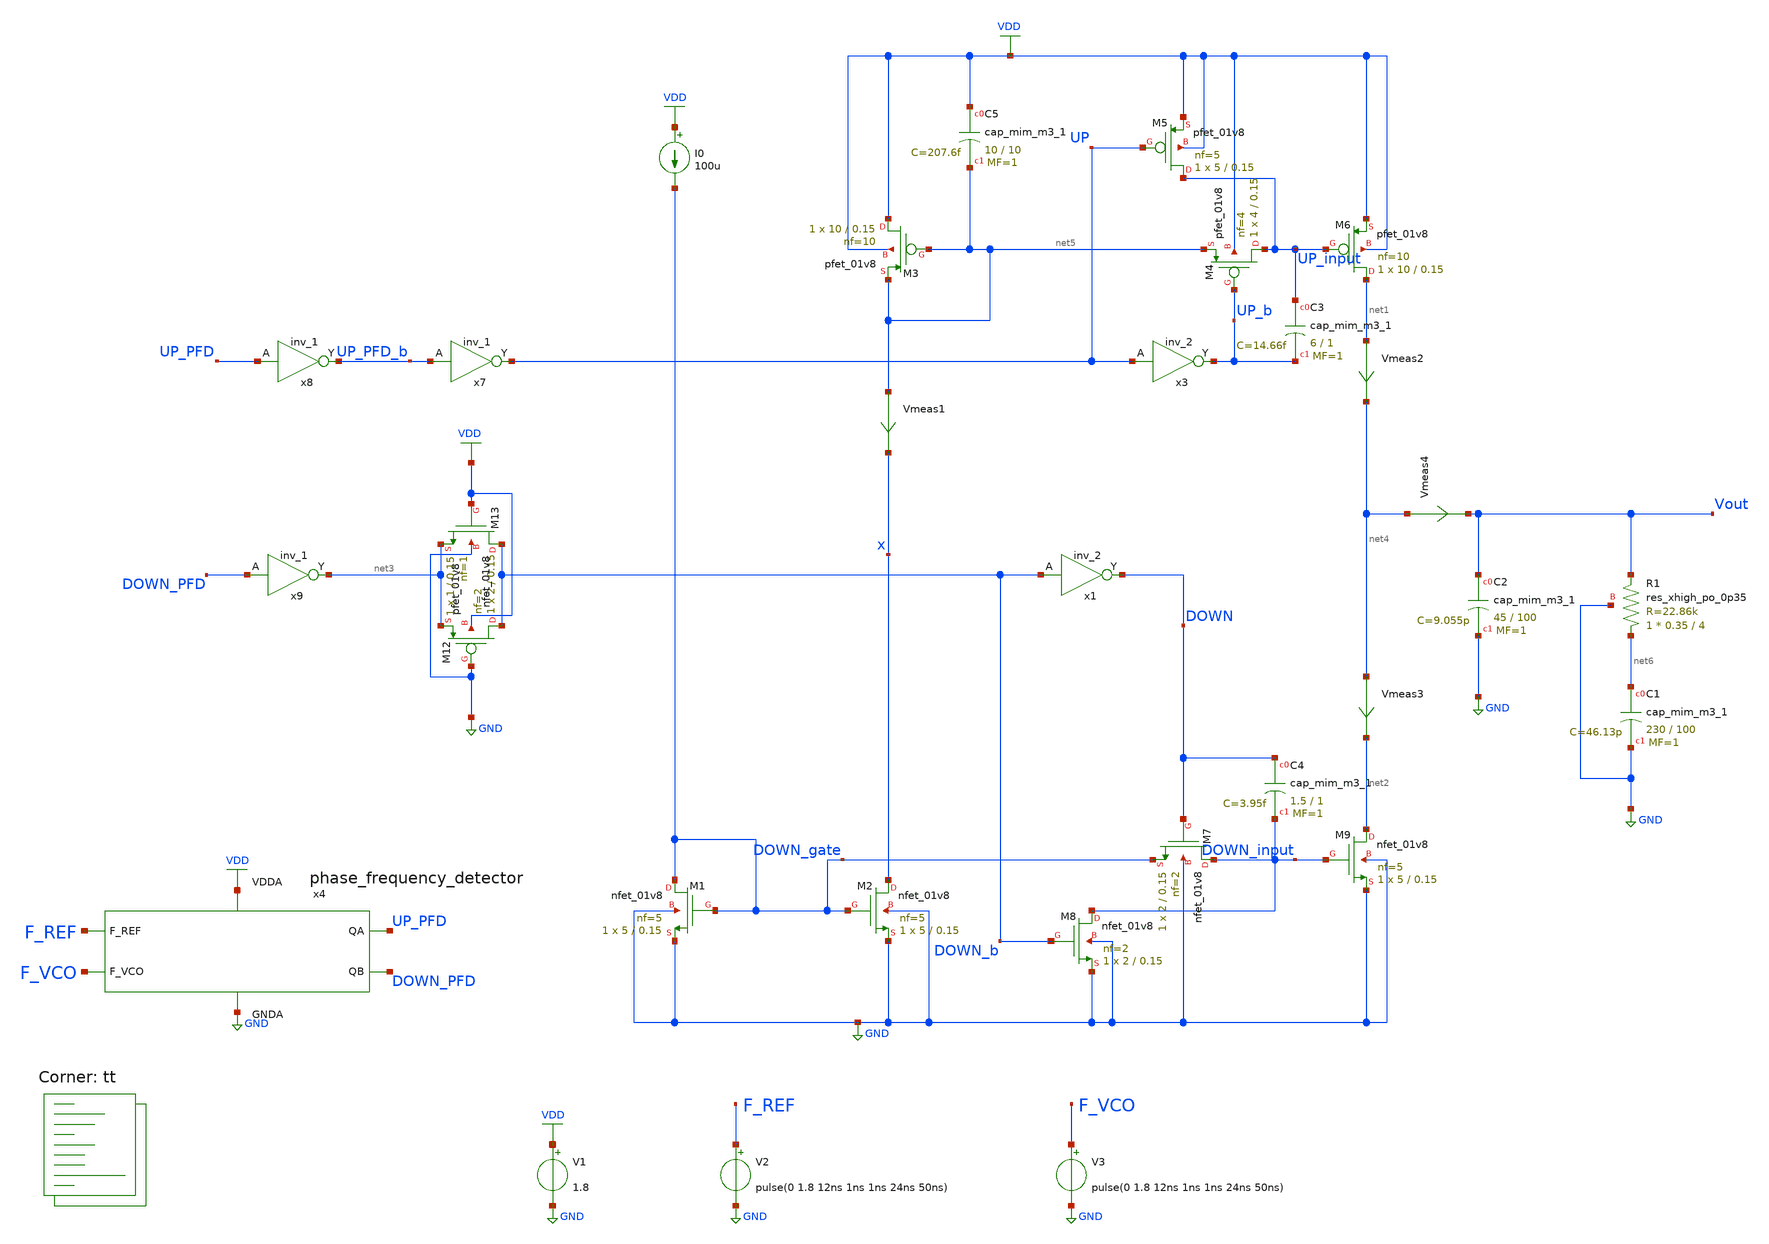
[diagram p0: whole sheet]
** sch_path: projects/pll/charge_pump/xschem_ngspice/pfd_charge_pump_5.sch
**.subckt pfd_charge_pump_5
XM1 DOWN_gate DOWN_gate GND GND sky130_fd_pr__nfet_01v8 L=0.15 W=5 nf=5 ad='int((nf+1)/2) * W/nf * 0.29'
+ as='int((nf+2)/2) * W/nf * 0.29' pd='2*int((nf+1)/2) * (W/nf + 0.29)' ps='2*int((nf+2)/2) * (W/nf + 0.29)'
+ nrd='0.29 / W' nrs='0.29 / W' sa=0 sb=0 sd=0 mult=1 m=1
XM2 x DOWN_gate GND GND sky130_fd_pr__nfet_01v8 L=0.15 W=5 nf=5 ad='int((nf+1)/2) * W/nf * 0.29' as='int((nf+2)/2) * W/nf * 0.29'
+ pd='2*int((nf+1)/2) * (W/nf + 0.29)' ps='2*int((nf+2)/2) * (W/nf + 0.29)' nrd='0.29 / W' nrs='0.29 / W'
+ sa=0 sb=0 sd=0 mult=1 m=1
XM3 VDD net5 net5 VDD sky130_fd_pr__pfet_01v8 L=0.15 W=10 nf=10 ad='int((nf+1)/2) * W/nf * 0.29' as='int((nf+2)/2) * W/nf * 0.29'
+ pd='2*int((nf+1)/2) * (W/nf + 0.29)' ps='2*int((nf+2)/2) * (W/nf + 0.29)' nrd='0.29 / W' nrs='0.29 / W'
+ sa=0 sb=0 sd=0 mult=1 m=1
V1 VDD GND 1.8
I0 VDD DOWN_gate 100u
Vmeas1 net5 x 0
.save i(vmeas1)
XM4 UP_input UP_b net5 VDD sky130_fd_pr__pfet_01v8 L=0.15 W=4 nf=4 ad='int((nf+1)/2) * W/nf * 0.29' as='int((nf+2)/2) * W/nf * 0.29'
+ pd='2*int((nf+1)/2) * (W/nf + 0.29)' ps='2*int((nf+2)/2) * (W/nf + 0.29)' nrd='0.29 / W' nrs='0.29 / W'
+ sa=0 sb=0 sd=0 mult=1 m=1
XM5 UP_input UP VDD VDD sky130_fd_pr__pfet_01v8 L=0.15 W=5 nf=5 ad='int((nf+1)/2) * W/nf * 0.29' as='int((nf+2)/2) * W/nf * 0.29'
+ pd='2*int((nf+1)/2) * (W/nf + 0.29)' ps='2*int((nf+2)/2) * (W/nf + 0.29)' nrd='0.29 / W' nrs='0.29 / W'
+ sa=0 sb=0 sd=0 mult=1 m=1
XM6 net1 UP_input VDD VDD sky130_fd_pr__pfet_01v8 L=0.15 W=10 nf=10 ad='int((nf+1)/2) * W/nf * 0.29'
+ as='int((nf+2)/2) * W/nf * 0.29' pd='2*int((nf+1)/2) * (W/nf + 0.29)' ps='2*int((nf+2)/2) * (W/nf + 0.29)'
+ nrd='0.29 / W' nrs='0.29 / W' sa=0 sb=0 sd=0 mult=1 m=1
Vmeas2 net1 net4 0
.save i(vmeas2)
XM7 DOWN_input DOWN DOWN_gate GND sky130_fd_pr__nfet_01v8 L=0.15 W=2 nf=2 ad='int((nf+1)/2) * W/nf * 0.29'
+ as='int((nf+2)/2) * W/nf * 0.29' pd='2*int((nf+1)/2) * (W/nf + 0.29)' ps='2*int((nf+2)/2) * (W/nf + 0.29)'
+ nrd='0.29 / W' nrs='0.29 / W' sa=0 sb=0 sd=0 mult=1 m=1
XM8 DOWN_input DOWN_b GND GND sky130_fd_pr__nfet_01v8 L=0.15 W=2 nf=2 ad='int((nf+1)/2) * W/nf * 0.29'
+ as='int((nf+2)/2) * W/nf * 0.29' pd='2*int((nf+1)/2) * (W/nf + 0.29)' ps='2*int((nf+2)/2) * (W/nf + 0.29)'
+ nrd='0.29 / W' nrs='0.29 / W' sa=0 sb=0 sd=0 mult=1 m=1
Vmeas3 net4 net2 0
.save i(vmeas3)
XM9 net2 DOWN_input GND GND sky130_fd_pr__nfet_01v8 L=0.15 W=5 nf=5 ad='int((nf+1)/2) * W/nf * 0.29'
+ as='int((nf+2)/2) * W/nf * 0.29' pd='2*int((nf+1)/2) * (W/nf + 0.29)' ps='2*int((nf+2)/2) * (W/nf + 0.29)'
+ nrd='0.29 / W' nrs='0.29 / W' sa=0 sb=0 sd=0 mult=1 m=1
x7 UP_PFD_b GND GND VDD VDD UP sky130_fd_sc_hd__inv_1
x8 UP_PFD GND GND VDD VDD UP_PFD_b sky130_fd_sc_hd__inv_1
x9 DOWN_PFD GND GND VDD VDD net3 sky130_fd_sc_hd__inv_1
x3 UP GND GND VDD VDD UP_b sky130_fd_sc_hd__inv_2
x1 DOWN_b GND GND VDD VDD DOWN sky130_fd_sc_hd__inv_2
XC2 Vout GND sky130_fd_pr__cap_mim_m3_1 W=45 L=100 MF=1 m=1
XC1 net6 GND sky130_fd_pr__cap_mim_m3_1 W=230 L=100 MF=1 m=1
V2 F_REF GND pulse(0 1.8 12ns 1ns 1ns 24ns 50ns)
V3 F_VCO GND pulse(0 1.8 12ns 1ns 1ns 24ns 50ns)
x4 F_REF F_VCO VDD UP_PFD DOWN_PFD GND phase_frequency_detector
Vmeas4 net4 Vout 0
.save i(vmeas4)
XC3 UP_input UP_b sky130_fd_pr__cap_mim_m3_1 W=6 L=1 MF=1 m=1
XR1 net6 Vout GND sky130_fd_pr__res_xhigh_po_0p35 L=4 mult=1 m=1
XC4 DOWN DOWN_input sky130_fd_pr__cap_mim_m3_1 W=1.5 L=1 MF=1 m=1
XC5 VDD net5 sky130_fd_pr__cap_mim_m3_1 W=10 L=10 MF=1 m=1
XM12 DOWN_b GND net3 VDD sky130_fd_pr__pfet_01v8 L=0.15 W=2 nf=2 ad='int((nf+1)/2) * W/nf * 0.29' as='int((nf+2)/2) * W/nf * 0.29'
+ pd='2*int((nf+1)/2) * (W/nf + 0.29)' ps='2*int((nf+2)/2) * (W/nf + 0.29)' nrd='0.29 / W' nrs='0.29 / W'
+ sa=0 sb=0 sd=0 mult=1 m=1
XM13 DOWN_b VDD net3 GND sky130_fd_pr__nfet_01v8 L=0.15 W=1 nf=1 ad='int((nf+1)/2) * W/nf * 0.29' as='int((nf+2)/2) * W/nf * 0.29'
+ pd='2*int((nf+1)/2) * (W/nf + 0.29)' ps='2*int((nf+2)/2) * (W/nf + 0.29)' nrd='0.29 / W' nrs='0.29 / W'
+ sa=0 sb=0 sd=0 mult=1 m=1
**** begin user architecture code
.lib $::SKYWATER_MODELS/sky130.lib.spice tt



.include /foss/pdks/sky130A/libs.ref/sky130_fd_sc_hd/spice/sky130_fd_sc_hd.spice

.option method=gear trtol1
.option wnflag=1
* .option savecurrents

* .temp = 75

.ic v(vout) = 1.2

.save  v(up_pfd) v(down_pfd) v(up_pfd_b) v(down_pfd_b) v(up) v(up_b) v(down) v(down_b) v(v2) v(x) v(y) v(z) v(vout) v(up_input) v(down_input) v(down_gate) v(opamp_out) v(x2.p_bias) v(x2.n_bias) v(x2.v_common_p) v(x2.v_common_n) v(x2.p_left) v(x2.p_right) v(x2.n_left) v(x2.n_right) v(f_ref) v(f_vco) v(x4.qa) v(x4.qa_b) v(x4.qb) v(x4.qb_b) v(x4.qa) v(x4.e) v(x4.e_b) v(x4.f) v(x4.f_b) v(x4.before_reset) v(x4.reset)


.control
  * save v(up_pfd) v(down_pfd) v(up_pfd_b) v(down_pfd_b) v(up) v(up_b) v(down) v(down_b) v(x)
+ v(vout) v(up_input) v(down_input)
  * save all

  tran 0.1ns 1us
  * dc v2 0 1.8 0.01
  remzerovec
  write pfd_charge_pump_5.raw
  * wrdata /foss/designs/my_design/projects/pll/charge_pump/xschem_ngspice/charge_pump2_QA.txt
+ v(osc)
  set appendwrite

.endc






**** end user architecture code
**.ends

* expanding   symbol:
*+  /foss/designs/my_design/projects/pll/pfd/xschem_ngspice/phase_frequency_detector.sym # of pins=6
** sym_path: projects/pll/pfd/xschem_ngspice/phase_frequency_detector.sym
** sch_path: projects/pll/pfd/xschem_ngspice/phase_frequency_detector.sch
.subckt phase_frequency_detector F_REF F_VCO VDDA QA QB GNDA
*.ipin F_REF
*.opin QA
*.ipin F_VCO
*.opin QB
*.ipin VDDA
*.ipin GNDA
x1 F_REF QA GNDA GNDA VDDA VDDA QA_b sky130_fd_sc_hd__nor2_1
x2 QA_b E GNDA GNDA VDDA VDDA QA sky130_fd_sc_hd__nor2_1
x3 QA_b E_b GNDA GNDA VDDA VDDA E sky130_fd_sc_hd__nor2_1
x4 E Reset GNDA GNDA VDDA VDDA E_b sky130_fd_sc_hd__nor2_1
x5 F_VCO QB GNDA GNDA VDDA VDDA QB_b sky130_fd_sc_hd__nor2_1
x6 QB_b F GNDA GNDA VDDA VDDA QB sky130_fd_sc_hd__nor2_1
x7 QB_b F_b GNDA GNDA VDDA VDDA F sky130_fd_sc_hd__nor2_1
x8 F Reset GNDA GNDA VDDA VDDA F_b sky130_fd_sc_hd__nor2_1
x9 QA QB GNDA GNDA VDDA VDDA before_Reset sky130_fd_sc_hd__nand2_1
x10 before_Reset GNDA GNDA VDDA VDDA net1 sky130_fd_sc_hd__inv_1
x11 net1 GNDA GNDA VDDA VDDA net2 sky130_fd_sc_hd__inv_1
x12 net2 GNDA GNDA VDDA VDDA net3 sky130_fd_sc_hd__inv_1
x13 net3 GNDA GNDA VDDA VDDA net4 sky130_fd_sc_hd__inv_1
x14 net4 GNDA GNDA VDDA VDDA Reset sky130_fd_sc_hd__inv_1
.ends

.GLOBAL VDD
.GLOBAL GND
.end
